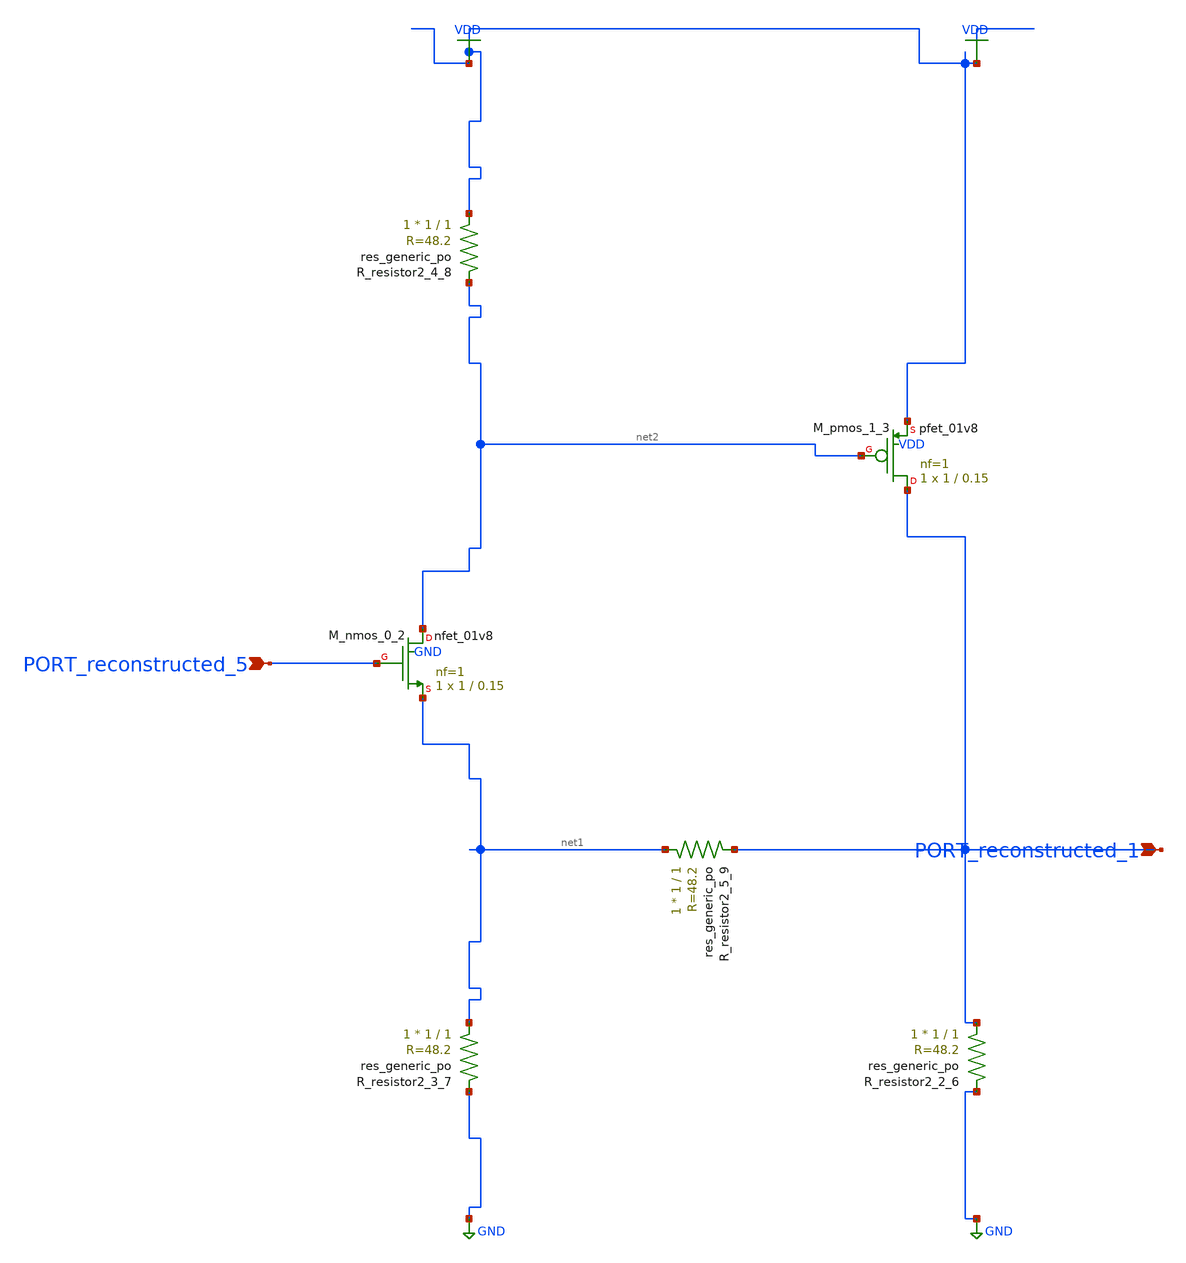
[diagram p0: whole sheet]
** sch_path: schematics/AMSNet/568.sch
**.subckt 568 PORT_reconstructed_5 PORT_reconstructed_1
*.ipin PORT_reconstructed_5
*.ipin PORT_reconstructed_1
XM_nmos_0_2 net2 PORT_reconstructed_5 net1 GND sky130_fd_pr__nfet_01v8 L=0.15 W=1 nf=1 ad='int((1 + 1)/2) * 1 / 1 * 0.29'
+ as='int((1 + 2)/2) * 1 / 1 * 0.29' pd='2*int((1 + 1)/2) * (1 / 1 + 0.29)' ps='2*int((1 + 2)/2) * (1 / 1 + 0.29)'
+ nrd='0.29 / 1 ' nrs='0.29 / 1 ' sa=0 sb=0 sd=0 mult=1 m=1
XM_pmos_1_3 PORT_reconstructed_1 net2 VDD VDD sky130_fd_pr__pfet_01v8 L=0.15 W=1 nf=1 ad='int((1 + 1)/2) * 1 / 1 * 0.29'
+ as='int((1 + 2)/2) * 1 / 1 * 0.29' pd='2*int((1 + 1)/2) * (1 / 1 + 0.29)' ps='2*int((1 + 2)/2) * (1 / 1 + 0.29)'
+ nrd='0.29 / 1 ' nrs='0.29 / 1 ' sa=0 sb=0 sd=0 mult=1 m=1
XR_resistor2_2_6 PORT_reconstructed_1 GND sky130_fd_pr__res_generic_po W=1 L=1 m=1
XR_resistor2_3_7 net1 GND sky130_fd_pr__res_generic_po W=1 L=1 m=1
XR_resistor2_4_8 VDD net2 sky130_fd_pr__res_generic_po W=1 L=1 m=1
XR_resistor2_5_9 net1 PORT_reconstructed_1 sky130_fd_pr__res_generic_po W=1 L=1 m=1
**.ends
.GLOBAL GND
.GLOBAL VDD
.end
